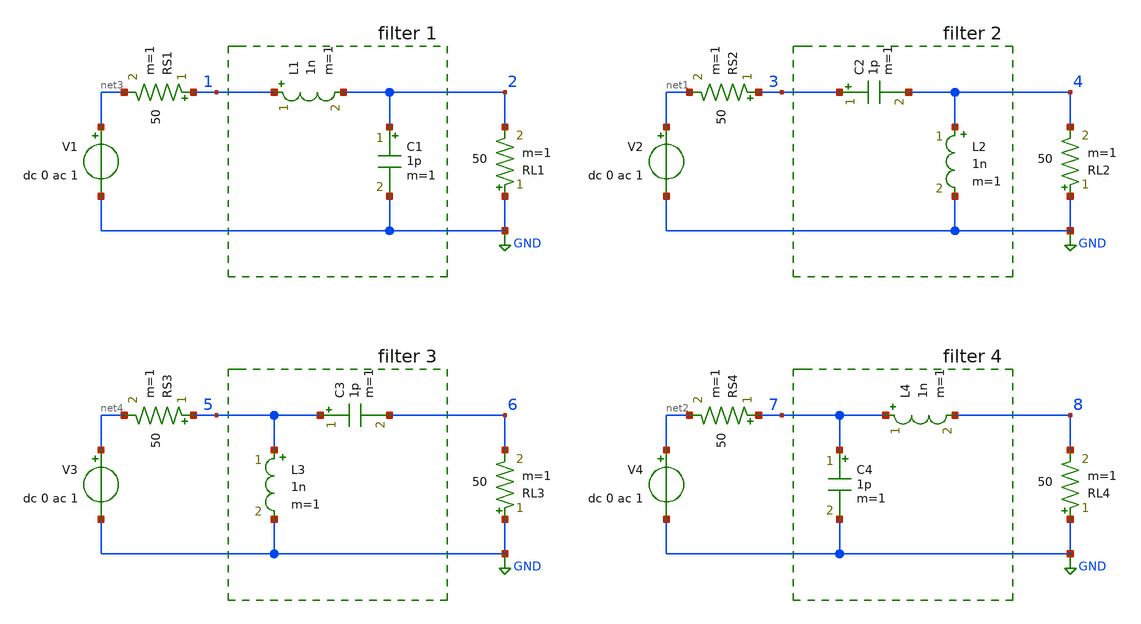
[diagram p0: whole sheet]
** sch_path: circuitos/exemplo03b.sch
**.subckt exemplo03b
V2 net1 GND dc 0 ac 1
RL2 GND 4 50 m=1
V3 net4 GND dc 0 ac 1
RL4 GND 8 50 m=1
RS2 3 net1 50 m=1
RS4 7 net2 50 m=1
C1 2 GND 1p m=1
V1 net3 GND dc 0 ac 1
RL1 GND 2 50 m=1
V4 net2 GND dc 0 ac 1
RL3 GND 6 50 m=1
L3 5 GND 1n m=1
RS1 1 net3 50 m=1
RS3 5 net4 50 m=1
L4 7 8 1n m=1
C2 3 4 1p m=1
L1 1 2 1n m=1
L2 4 GND 1n m=1
C3 5 6 1p m=1
C4 7 GND 1p m=1
**** begin user architecture code

.ac lin 1001 100 10G

**** end user architecture code
**.ends
.GLOBAL GND
.end
